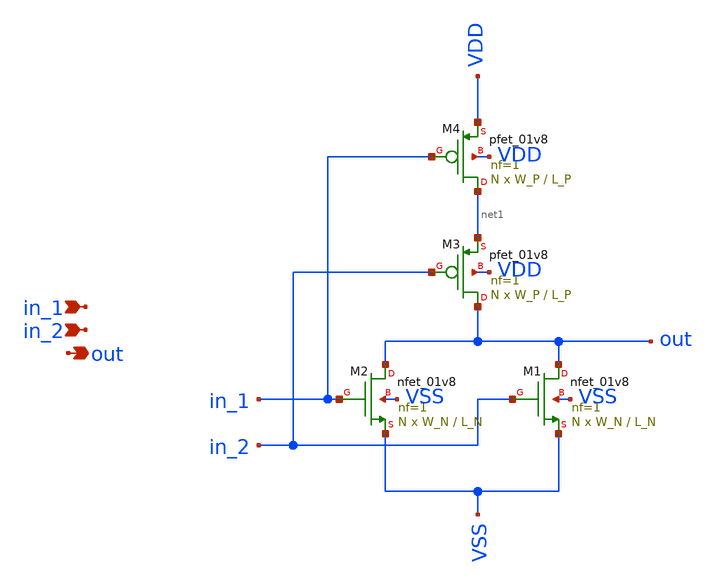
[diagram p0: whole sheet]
** sch_path: design/schematic/nor2.sch
**.subckt nor2 in_1 in_2 out
*.ipin in_1
*.ipin in_2
*.opin out
XM1 out in_2 VSS VSS sky130_fd_pr__nfet_01v8 L=L_N W=W_N nf=1 ad='int((nf+1)/2) * W/nf * 0.29' as='int((nf+2)/2) * W/nf * 0.29'
+ pd='2*int((nf+1)/2) * (W/nf + 0.29)' ps='2*int((nf+2)/2) * (W/nf + 0.29)' nrd='0.29 / W' nrs='0.29 / W'
+ sa=0 sb=0 sd=0 mult=N m=N
XM2 out in_1 VSS VSS sky130_fd_pr__nfet_01v8 L=L_N W=W_N nf=1 ad='int((nf+1)/2) * W/nf * 0.29' as='int((nf+2)/2) * W/nf * 0.29'
+ pd='2*int((nf+1)/2) * (W/nf + 0.29)' ps='2*int((nf+2)/2) * (W/nf + 0.29)' nrd='0.29 / W' nrs='0.29 / W'
+ sa=0 sb=0 sd=0 mult=N m=N
XM3 out in_2 net1 VDD sky130_fd_pr__pfet_01v8 L=L_P W=W_P nf=1 ad='int((nf+1)/2) * W/nf * 0.29' as='int((nf+2)/2) * W/nf * 0.29'
+ pd='2*int((nf+1)/2) * (W/nf + 0.29)' ps='2*int((nf+2)/2) * (W/nf + 0.29)' nrd='0.29 / W' nrs='0.29 / W'
+ sa=0 sb=0 sd=0 mult=N m=N
XM4 net1 in_1 VDD VDD sky130_fd_pr__pfet_01v8 L=L_P W=W_P nf=1 ad='int((nf+1)/2) * W/nf * 0.29' as='int((nf+2)/2) * W/nf * 0.29'
+ pd='2*int((nf+1)/2) * (W/nf + 0.29)' ps='2*int((nf+2)/2) * (W/nf + 0.29)' nrd='0.29 / W' nrs='0.29 / W'
+ sa=0 sb=0 sd=0 mult=N m=N
**.ends
.end
